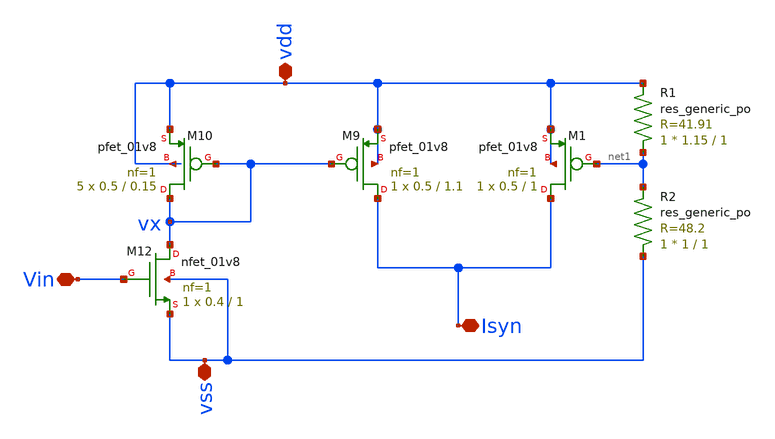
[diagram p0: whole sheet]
** sch_path: Neuron/ultralif/syn_pos.sch
**.subckt syn_pos Vin vdd vss Isyn
*.iopin Vin
*.iopin vdd
*.iopin vss
*.iopin Isyn
XM9 Isyn vx vdd vdd sky130_fd_pr__pfet_01v8 L=1.1 W=0.5 nf=1 ad='int((nf+1)/2) * W/nf * 0.29' as='int((nf+2)/2) * W/nf * 0.29'
+ pd='2*int((nf+1)/2) * (W/nf + 0.29)' ps='2*int((nf+2)/2) * (W/nf + 0.29)' nrd='0.29 / W' nrs='0.29 / W'
+ sa=0 sb=0 sd=0 mult=1 m=1
XM10 vx vx vdd vdd sky130_fd_pr__pfet_01v8 L=0.15 W=0.5 nf=1 ad='int((nf+1)/2) * W/nf * 0.29' as='int((nf+2)/2) * W/nf * 0.29'
+ pd='2*int((nf+1)/2) * (W/nf + 0.29)' ps='2*int((nf+2)/2) * (W/nf + 0.29)' nrd='0.29 / W' nrs='0.29 / W'
+ sa=0 sb=0 sd=0 mult=5 m=5
XM12 vx Vin vss vss sky130_fd_pr__nfet_01v8 L=1 W=0.4 nf=1 ad='int((1 + 1)/2) * 0.4 / 1 * 0.29' as='int((1 + 2)/2) * 0.4 / 1 * 0.29'
+ pd='2*int((1 + 1)/2) * (0.4 / 1 + 0.29)' ps='2*int((1 + 2)/2) * (0.4 / 1 + 0.29)' nrd='0.29 / 0.4 ' nrs='0.29 / 0.4 '
+ sa=0 sb=0 sd=0 mult=1 m=1
XM1 Isyn net1 vdd vdd sky130_fd_pr__pfet_01v8 L=1 W=0.5 nf=1 ad='int((nf+1)/2) * W/nf * 0.29' as='int((nf+2)/2) * W/nf * 0.29'
+ pd='2*int((nf+1)/2) * (W/nf + 0.29)' ps='2*int((nf+2)/2) * (W/nf + 0.29)' nrd='0.29 / W' nrs='0.29 / W'
+ sa=0 sb=0 sd=0 mult=1 m=1
XR1 net1 vdd sky130_fd_pr__res_generic_po W=1.15 L=1 m=1
XR2 vss net1 sky130_fd_pr__res_generic_po W=1 L=1 m=1
**.ends
.end
